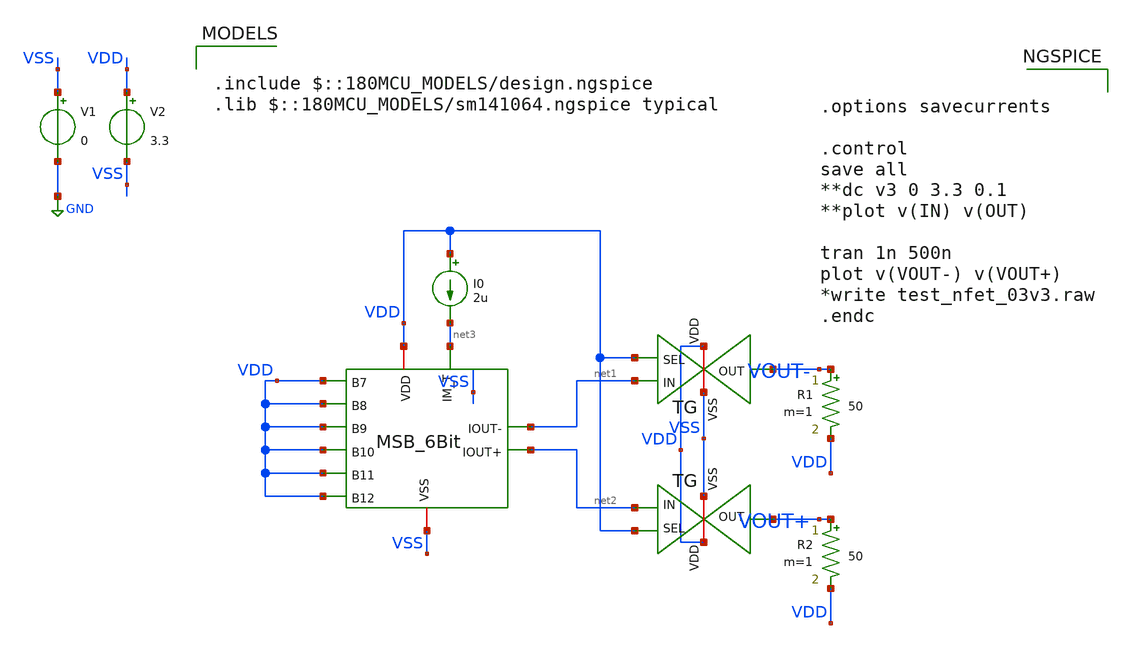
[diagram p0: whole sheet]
** sch_path: DAC_PAKISTAN_01/Pakistan1_Xschem/CURRENT_TEST.sch
**.subckt CURRENT_TEST
x1 VSS VDD VDD VDD VDD VDD VDD net3 VDD net1 net2 MSB_6Bit
x2 VDD VDD VSS VOUT- net1 TG
x3 VDD VDD VSS VOUT+ net2 TG
V1 VSS GND 0
V2 VDD VSS 3.3
I0 VDD net3 2u
R1 VOUT- VDD 50 m=1
R2 VOUT+ VDD 50 m=1
**** begin user architecture code

.include $::180MCU_MODELS/design.ngspice
.lib $::180MCU_MODELS/sm141064.ngspice typical



.options savecurrents

.control
save all
**dc v3 0 3.3 0.1
**plot v(IN) v(OUT)

tran 1n 500n
plot v(VOUT-) v(VOUT+)
*write test_nfet_03v3.raw
.endc


**** end user architecture code
**.ends
.GLOBAL GND
.end
